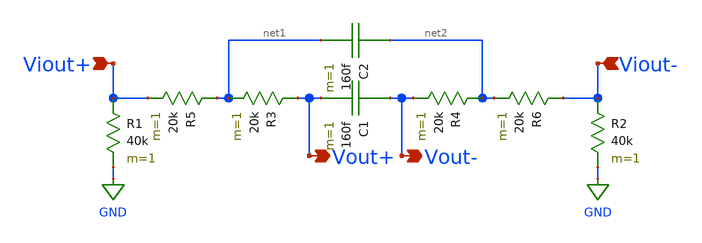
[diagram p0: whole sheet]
** sch_path: simulation/filter/filter.sch
**.subckt filter Vout+ Vout- Viout+ Viout-
*.opin Vout+
*.opin Vout-
*.ipin Viout+
*.ipin Viout-
R1 Viout+ GND 40k m=1
R2 Viout- GND 40k m=1
R3 Vout+ net1 20k m=1
R4 net2 Vout- 20k m=1
C1 Vout- Vout+ 160f m=1
R5 net1 Viout+ 20k m=1
R6 Viout- net2 20k m=1
C2 net2 net1 160f m=1
**.ends
.GLOBAL GND
.end
